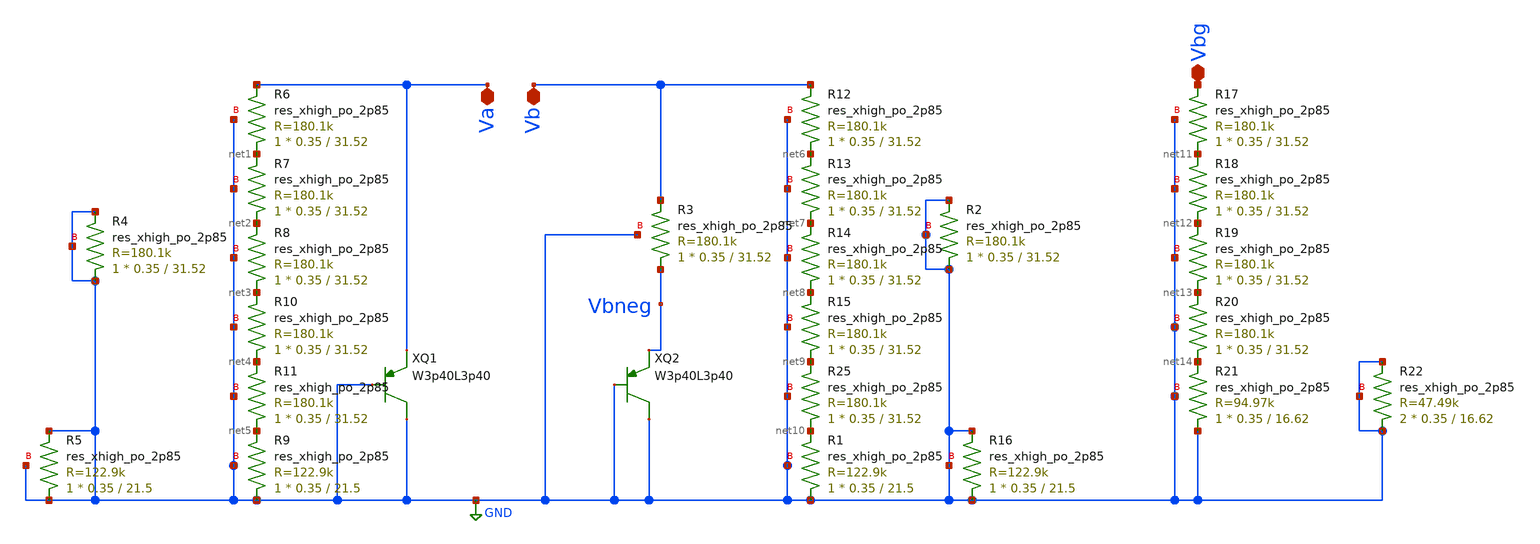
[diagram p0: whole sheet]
** sch_path: schematics/bandgapCore.sch
**.subckt bandgapCore Va Vb Vbg
*.iopin Va
*.iopin Vb
*.iopin Vbg
XR3 Vbneg Vb GND sky130_fd_pr__res_xhigh_po_2p85 L=31.52 mult=1 m=1
XQ1 GND GND Va sky130_fd_pr__pnp_05v5 m=1
XQ2 GND GND Vbneg sky130_fd_pr__pnp_05v5 m=39
XR4 GND GND GND sky130_fd_pr__res_xhigh_po_2p85 L=31.52 mult=1 m=1
XR2 GND GND GND sky130_fd_pr__res_xhigh_po_2p85 L=31.52 mult=1 m=1
XR6 net1 Va GND sky130_fd_pr__res_xhigh_po_2p85 L=31.52 mult=1 m=1
XR7 net2 net1 GND sky130_fd_pr__res_xhigh_po_2p85 L=31.52 mult=1 m=1
XR8 net3 net2 GND sky130_fd_pr__res_xhigh_po_2p85 L=31.52 mult=1 m=1
XR10 net4 net3 GND sky130_fd_pr__res_xhigh_po_2p85 L=31.52 mult=1 m=1
XR11 net5 net4 GND sky130_fd_pr__res_xhigh_po_2p85 L=31.52 mult=1 m=1
XR9 GND net5 GND sky130_fd_pr__res_xhigh_po_2p85 L=21.5 mult=1 m=1
XR12 net6 Vb GND sky130_fd_pr__res_xhigh_po_2p85 L=31.52 mult=1 m=1
XR13 net7 net6 GND sky130_fd_pr__res_xhigh_po_2p85 L=31.52 mult=1 m=1
XR14 net8 net7 GND sky130_fd_pr__res_xhigh_po_2p85 L=31.52 mult=1 m=1
XR15 net9 net8 GND sky130_fd_pr__res_xhigh_po_2p85 L=31.52 mult=1 m=1
XR25 net10 net9 GND sky130_fd_pr__res_xhigh_po_2p85 L=31.52 mult=1 m=1
XR1 GND net10 GND sky130_fd_pr__res_xhigh_po_2p85 L=21.5 mult=1 m=1
XR5 GND GND GND sky130_fd_pr__res_xhigh_po_2p85 L=21.5 mult=1 m=1
XR16 GND GND GND sky130_fd_pr__res_xhigh_po_2p85 L=21.5 mult=1 m=1
XR17 net11 Vbg GND sky130_fd_pr__res_xhigh_po_2p85 L=31.52 mult=1 m=1
XR18 net12 net11 GND sky130_fd_pr__res_xhigh_po_2p85 L=31.52 mult=1 m=1
XR19 net13 net12 GND sky130_fd_pr__res_xhigh_po_2p85 L=31.52 mult=1 m=1
XR20 net14 net13 GND sky130_fd_pr__res_xhigh_po_2p85 L=31.52 mult=1 m=1
XR21 GND net14 GND sky130_fd_pr__res_xhigh_po_2p85 L=16.62 mult=1 m=1
XR22 GND GND GND sky130_fd_pr__res_xhigh_po_2p85 L=16.62 mult=2 m=2
**.ends
.GLOBAL GND
.end
